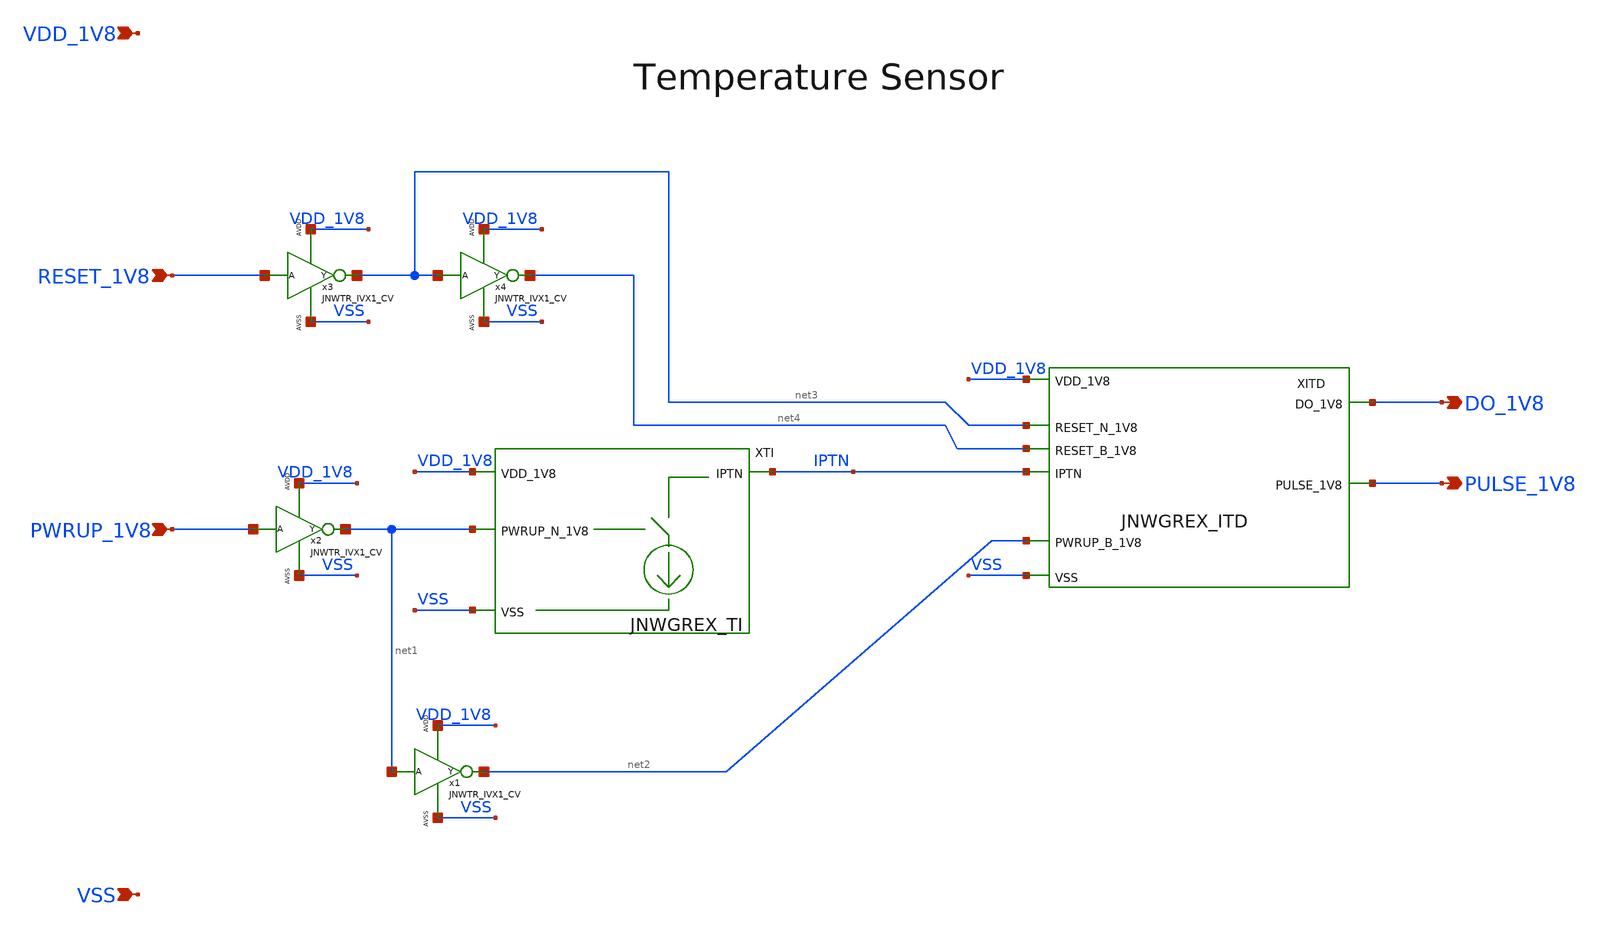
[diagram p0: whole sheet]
** sch_path: design/JNW_GREX_SKY130A/JNW_GREX.sch
**.subckt JNW_GREX VDD_1V8 VSS PWRUP_1V8 RESET_1V8 DO_1V8 PULSE_1V8
*.ipin VDD_1V8
*.ipin VSS
*.ipin PWRUP_1V8
*.ipin RESET_1V8
*.opin DO_1V8
*.opin PULSE_1V8
XTI VDD_1V8 IPTN VSS net1 JNWGREX_TI
x2 PWRUP_1V8 net1 VDD_1V8 VSS JNWTR_IVX1_CV
XITD VDD_1V8 net3 net2 IPTN DO_1V8 PULSE_1V8 net4 VSS JNWGREX_ITD
x1 net1 net2 VDD_1V8 VSS JNWTR_IVX1_CV
x3 RESET_1V8 net3 VDD_1V8 VSS JNWTR_IVX1_CV
x4 net3 net4 VDD_1V8 VSS JNWTR_IVX1_CV
**.ends
.end
